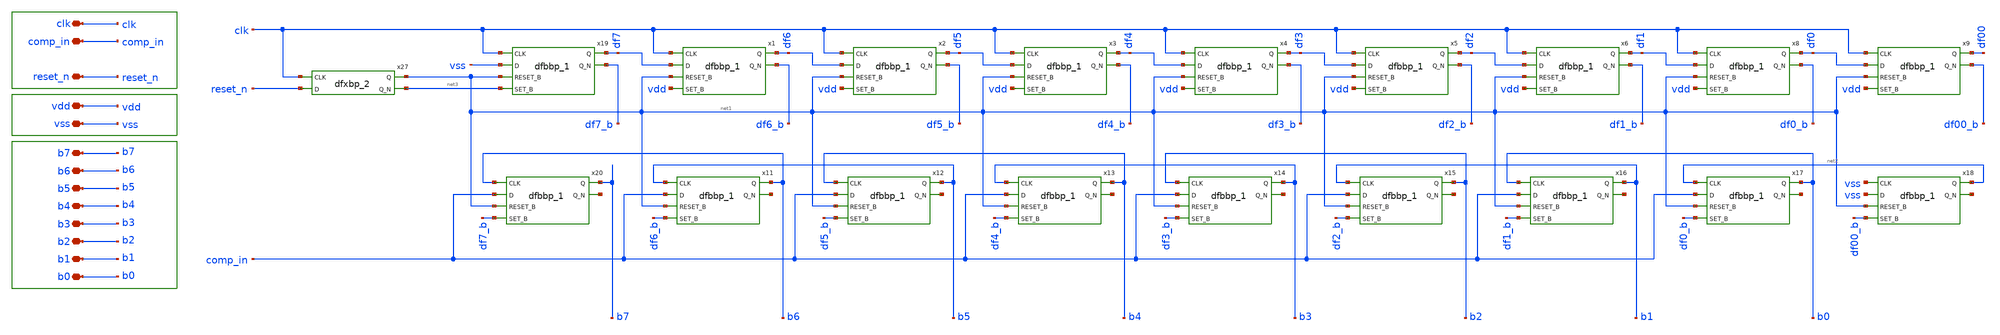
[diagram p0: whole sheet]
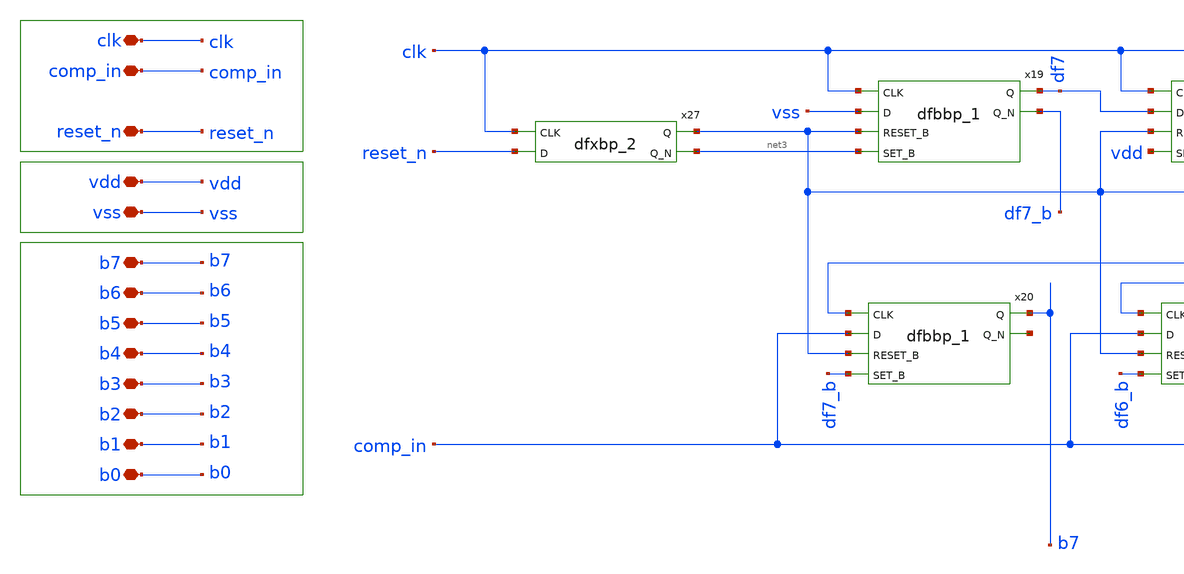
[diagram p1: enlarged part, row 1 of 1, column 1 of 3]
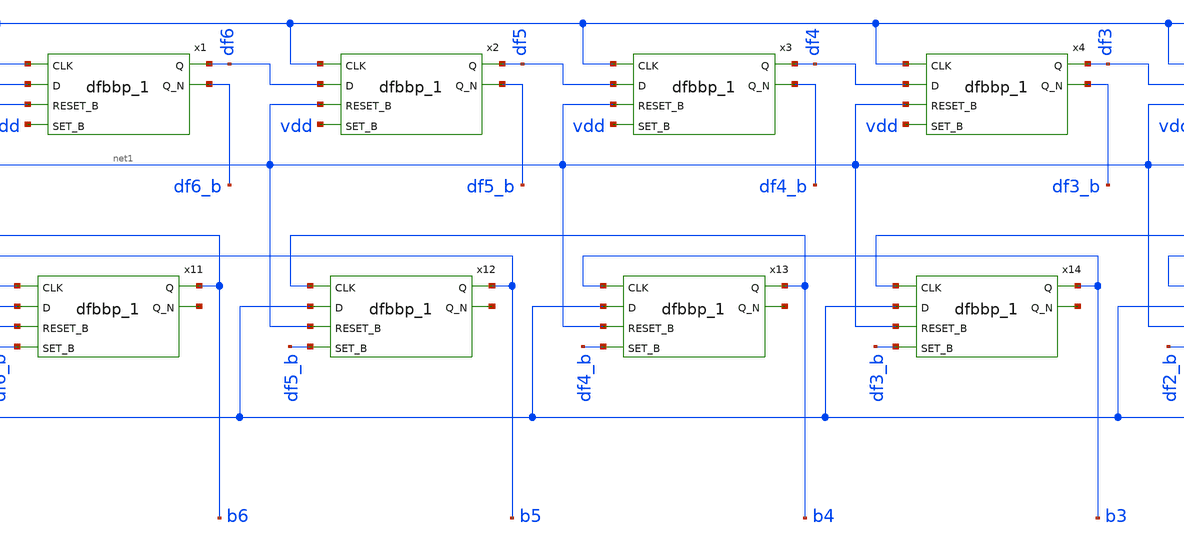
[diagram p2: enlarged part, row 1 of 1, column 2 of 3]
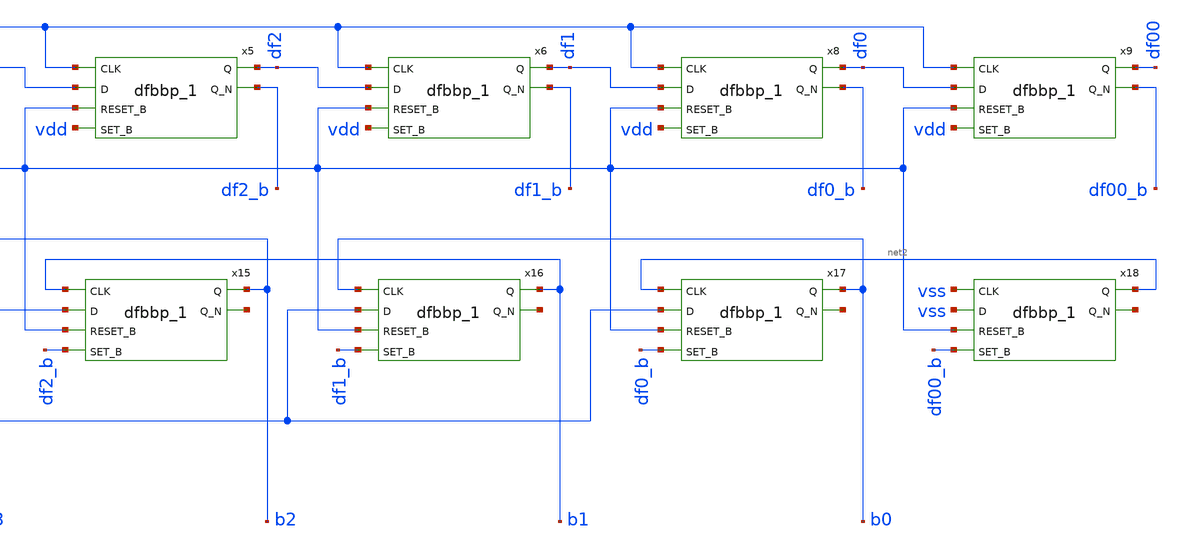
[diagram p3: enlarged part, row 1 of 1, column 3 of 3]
** sch_path: xschem/sar_logic/sarlogic.sch
**.subckt sarlogic vdd clk b7 b6 b5 b4 b3 b2 b1 b0 comp_in vss reset_n
*.iopin vdd
*.iopin clk
*.iopin b7
*.iopin b6
*.iopin b5
*.iopin b4
*.iopin b3
*.iopin b2
*.iopin b1
*.iopin b0
*.iopin comp_in
*.iopin vss
*.iopin reset_n
x1 clk df7 net1 vdd vss vss vdd vdd df6 df6_b sky130_fd_sc_hd__dfbbp_1
x2 clk df6 net1 vdd vss vss vdd vdd df5 df5_b sky130_fd_sc_hd__dfbbp_1
x3 clk df5 net1 vdd vss vss vdd vdd df4 df4_b sky130_fd_sc_hd__dfbbp_1
x4 clk df4 net1 vdd vss vss vdd vdd df3 df3_b sky130_fd_sc_hd__dfbbp_1
x5 clk df3 net1 vdd vss vss vdd vdd df2 df2_b sky130_fd_sc_hd__dfbbp_1
x6 clk df2 net1 vdd vss vss vdd vdd df1 df1_b sky130_fd_sc_hd__dfbbp_1
x8 clk df1 net1 vdd vss vss vdd vdd df0 df0_b sky130_fd_sc_hd__dfbbp_1
x9 clk df0 net1 vdd vss vss vdd vdd df00 df00_b sky130_fd_sc_hd__dfbbp_1
x11 b5 comp_in net1 df6_b vss vss vdd vdd b6 net4 sky130_fd_sc_hd__dfbbp_1
x12 b4 comp_in net1 df5_b vss vss vdd vdd b5 net5 sky130_fd_sc_hd__dfbbp_1
x13 b3 comp_in net1 df4_b vss vss vdd vdd b4 net6 sky130_fd_sc_hd__dfbbp_1
x14 b2 comp_in net1 df3_b vss vss vdd vdd b3 net7 sky130_fd_sc_hd__dfbbp_1
x15 b1 comp_in net1 df2_b vss vss vdd vdd b2 net8 sky130_fd_sc_hd__dfbbp_1
x16 b0 comp_in net1 df1_b vss vss vdd vdd b1 net9 sky130_fd_sc_hd__dfbbp_1
x17 net2 comp_in net1 df0_b vss vss vdd vdd b0 net10 sky130_fd_sc_hd__dfbbp_1
x18 vss vss net1 df00_b vss vss vdd vdd net2 net11 sky130_fd_sc_hd__dfbbp_1
x19 clk vss net1 net3 vss vss vdd vdd df7 df7_b sky130_fd_sc_hd__dfbbp_1
x20 b6 comp_in net1 df7_b vss vss vdd vdd b7 net12 sky130_fd_sc_hd__dfbbp_1
x27 clk reset_n vss vss vdd vdd net1 net3 sky130_fd_sc_hd__dfxbp_2
**.ends
.end
